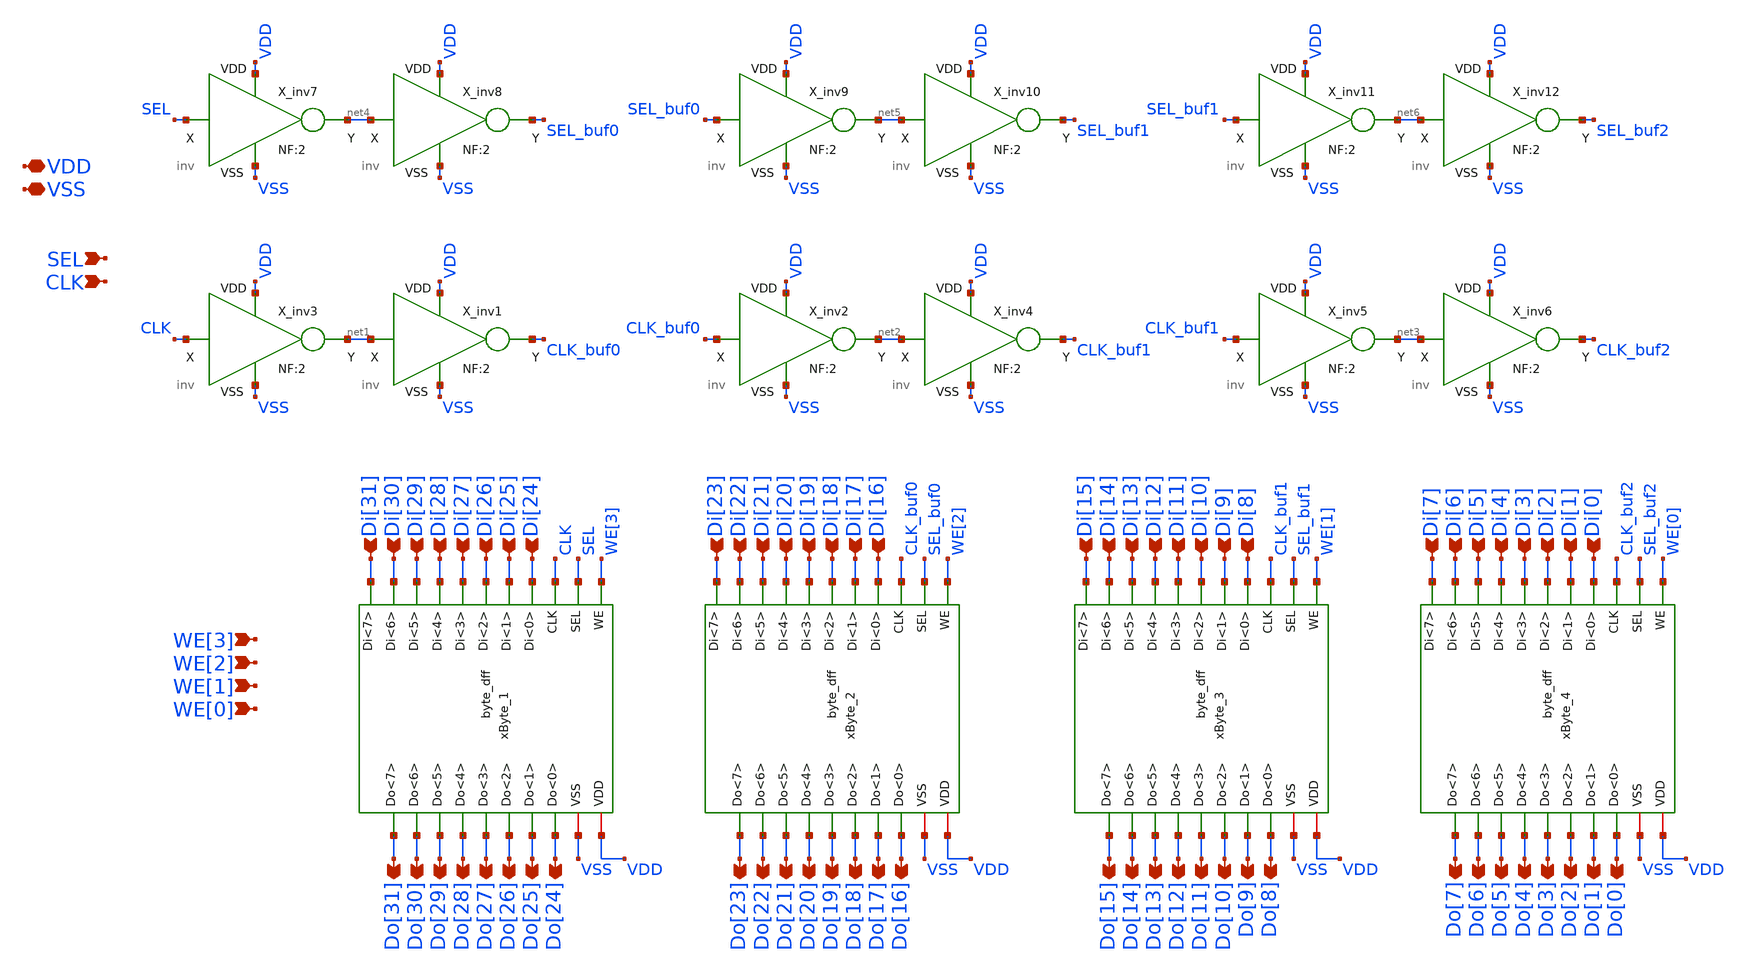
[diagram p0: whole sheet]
** sch_path: xschem_lib/sylee21/word.sch
**.subckt word SEL VDD VSS CLK Di[31] Di[30] Di[29] Di[28] Di[27] Di[26] Di[25] Di[24] Do[31] Do[30]
*+ Do[29] Do[28] Do[27] Do[26] Do[25] Do[24] Di[23] Di[22] Di[21] Di[20] Di[19] Di[18] Di[17] Di[16] Do[23]
*+ Do[22] Do[21] Do[20] Do[19] Do[18] Do[17] Do[16] Di[15] Di[14] Di[13] Di[12] Di[11] Di[10] Di[9] Di[8]
*+ Do[15] Do[14] Do[13] Do[12] Do[11] Do[10] Do[9] Do[8] Di[7] Di[6] Di[5] Di[4] Di[3] Di[2] Di[1] Di[0]
*+ Do[7] Do[6] Do[5] Do[4] Do[3] Do[2] Do[1] Do[0] WE[0] WE[1] WE[2] WE[3]
*.ipin SEL
*.iopin VDD
*.iopin VSS
*.ipin CLK
*.ipin Di[31]
*.ipin Di[30]
*.ipin Di[29]
*.ipin Di[28]
*.ipin Di[27]
*.ipin Di[26]
*.ipin Di[25]
*.ipin Di[24]
*.opin Do[31]
*.opin Do[30]
*.opin Do[29]
*.opin Do[28]
*.opin Do[27]
*.opin Do[26]
*.opin Do[25]
*.opin Do[24]
*.ipin Di[23]
*.ipin Di[22]
*.ipin Di[21]
*.ipin Di[20]
*.ipin Di[19]
*.ipin Di[18]
*.ipin Di[17]
*.ipin Di[16]
*.opin Do[23]
*.opin Do[22]
*.opin Do[21]
*.opin Do[20]
*.opin Do[19]
*.opin Do[18]
*.opin Do[17]
*.opin Do[16]
*.ipin Di[15]
*.ipin Di[14]
*.ipin Di[13]
*.ipin Di[12]
*.ipin Di[11]
*.ipin Di[10]
*.ipin Di[9]
*.ipin Di[8]
*.opin Do[15]
*.opin Do[14]
*.opin Do[13]
*.opin Do[12]
*.opin Do[11]
*.opin Do[10]
*.opin Do[9]
*.opin Do[8]
*.ipin Di[7]
*.ipin Di[6]
*.ipin Di[5]
*.ipin Di[4]
*.ipin Di[3]
*.ipin Di[2]
*.ipin Di[1]
*.ipin Di[0]
*.opin Do[7]
*.opin Do[6]
*.opin Do[5]
*.opin Do[4]
*.opin Do[3]
*.opin Do[2]
*.opin Do[1]
*.opin Do[0]
*.ipin WE[0]
*.ipin WE[1]
*.ipin WE[2]
*.ipin WE[3]
X_inv3 CLK VDD VSS net1 inv NF=2
X_inv1 net1 VDD VSS CLK_buf0 inv NF=2
X_inv2 CLK_buf0 VDD VSS net2 inv NF=2
X_inv4 net2 VDD VSS CLK_buf1 inv NF=2
X_inv5 CLK_buf1 VDD VSS net3 inv NF=2
X_inv6 net3 VDD VSS CLK_buf2 inv NF=2
X_inv7 SEL VDD VSS net4 inv NF=2
X_inv8 net4 VDD VSS SEL_buf0 inv NF=2
X_inv9 SEL_buf0 VDD VSS net5 inv NF=2
X_inv10 net5 VDD VSS SEL_buf1 inv NF=2
X_inv11 SEL_buf1 VDD VSS net6 inv NF=2
X_inv12 net6 VDD VSS SEL_buf2 inv NF=2
xByte_1 VDD VSS WE[3] Di[27] Di[31] Do[27] Do[31] CLK SEL Di[26] Di[30] Do[26] Do[30] Di[29] Di[25]
+ Do[29] Do[25] Di[28] Do[28] Di[24] Do[24] byte_dff NF=2
xByte_2 VDD VSS WE[2] Di[19] Di[23] Do[19] Do[23] CLK_buf0 SEL_buf0 Di[18] Di[22] Do[18] Do[22]
+ Di[21] Di[17] Do[21] Do[17] Di[20] Do[20] Di[16] Do[16] byte_dff NF=2
xByte_3 VDD VSS WE[1] Di[11] Di[15] Do[11] Do[15] CLK_buf1 SEL_buf1 Di[10] Di[14] Do[10] Do[14]
+ Di[13] Di[9] Do[13] Do[9] Di[12] Do[12] Di[8] Do[8] byte_dff NF=2
xByte_4 VDD VSS WE[0] Di[3] Di[7] Do[3] Do[7] CLK_buf2 SEL_buf2 Di[2] Di[6] Do[2] Do[6] Di[5] Di[1]
+ Do[5] Do[1] Di[4] Do[4] Di[0] Do[0] byte_dff NF=2
**.ends
.end
